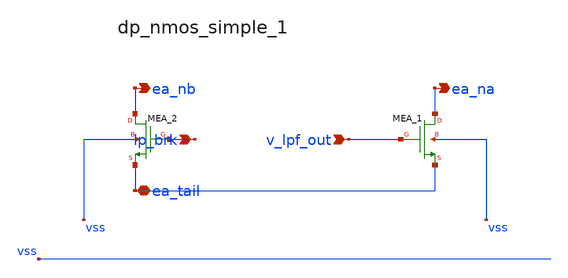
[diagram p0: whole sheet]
** sch_path: analog-db/raw/ldo_005_buffered_ref/hier/blocks/dp_nmos_simple_1.sch
**.subckt dp_nmos_simple_1 lp_brk v_lpf_out ea_tail ea_nb ea_na
*.ipin lp_brk
*.ipin v_lpf_out
*.iopin ea_tail
*.opin ea_nb
*.opin ea_na
XMEA_1 ea_na v_lpf_out ea_tail vss sg13_hv_nmos w=x_dut_xmea_1_w l=x_dut_xmea_1_l ng=1 m=1
XMEA_2 ea_nb lp_brk ea_tail vss sg13_hv_nmos w=x_dut_xmea_2_w l=x_dut_xmea_2_l ng=1 m=1
**.ends
.end
